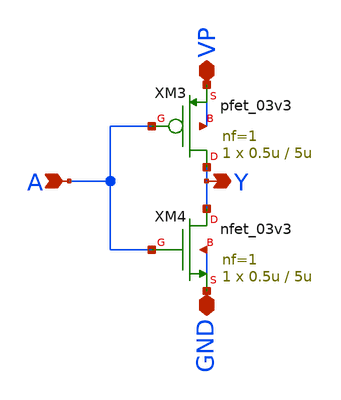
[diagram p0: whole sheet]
** sch_path: Designs/inverter.sch
**.subckt inverter A VP GND Y
*.ipin A
*.iopin VP
*.iopin GND
*.opin Y
XM3 Y A VP VP pfet_03v3 L=5u W=0.5u nf=1 ad='int((nf+1)/2) * W/nf * 0.18u' as='int((nf+2)/2) * W/nf * 0.18u'
+ pd='2*int((nf+1)/2) * (W/nf + 0.18u)' ps='2*int((nf+2)/2) * (W/nf + 0.18u)' nrd='0.18u / W' nrs='0.18u / W'
+ sa=0 sb=0 sd=0 m=1
XM4 Y A GND GND nfet_03v3 L=5u W=0.5u nf=1 ad='int((nf+1)/2) * W/nf * 0.18u' as='int((nf+2)/2) * W/nf * 0.18u'
+ pd='2*int((nf+1)/2) * (W/nf + 0.18u)' ps='2*int((nf+2)/2) * (W/nf + 0.18u)' nrd='0.18u / W' nrs='0.18u / W'
+ sa=0 sb=0 sd=0 m=1
**.ends
.end
